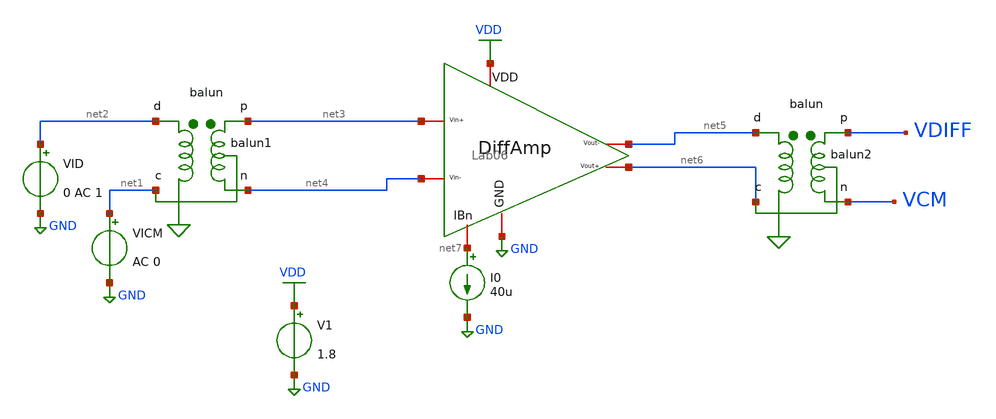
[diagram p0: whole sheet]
** sch_path: ITI_Labs/Lab6/Design/Lab06_Diff_Amp.sch
**.subckt Lab06_Diff_Amp
x1 VDD net7 net3 net4 net5 net6 GND Lab06
Xbalun1 net2 net1 net3 net4 balun
Xbalun2 net5 net6 VDIFF VCM balun
V1 VDD GND 1.8
I0 net7 GND 40u
VICM net1 GND AC 0
VID net2 GND 0 AC 1
**.ends
.GLOBAL VDD
.GLOBAL GND
.end
